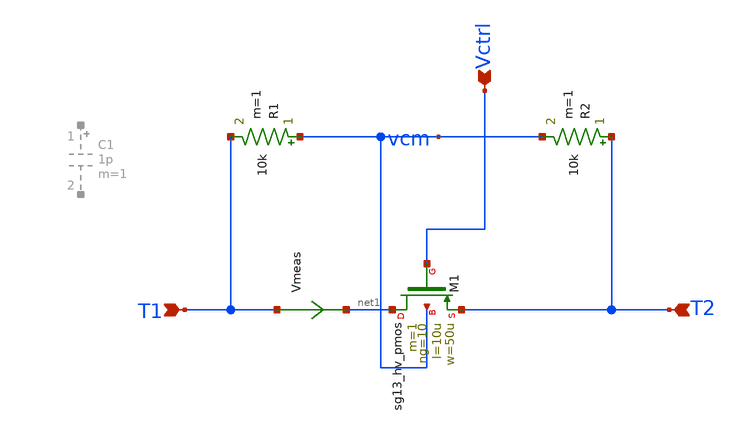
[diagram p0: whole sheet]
** sch_path: macros/heichips26_analog_project/macros/vcr_bisection/schematic/xschem/vcr_bisection.sch
**.subckt vcr_bisection T1 T2 Vctrl
*.ipin T1
*.ipin T2
*.ipin Vctrl
R1 vcm T1 10k m=1
R2 T2 vcm 10k m=1
Vmeas T1 net1 0
.save i(vmeas)
XM1 net1 Vctrl T2 vcm sg13_hv_pmos w=50u l=10u ng=10 m=1 mm_ok=1
**.ends
.end
